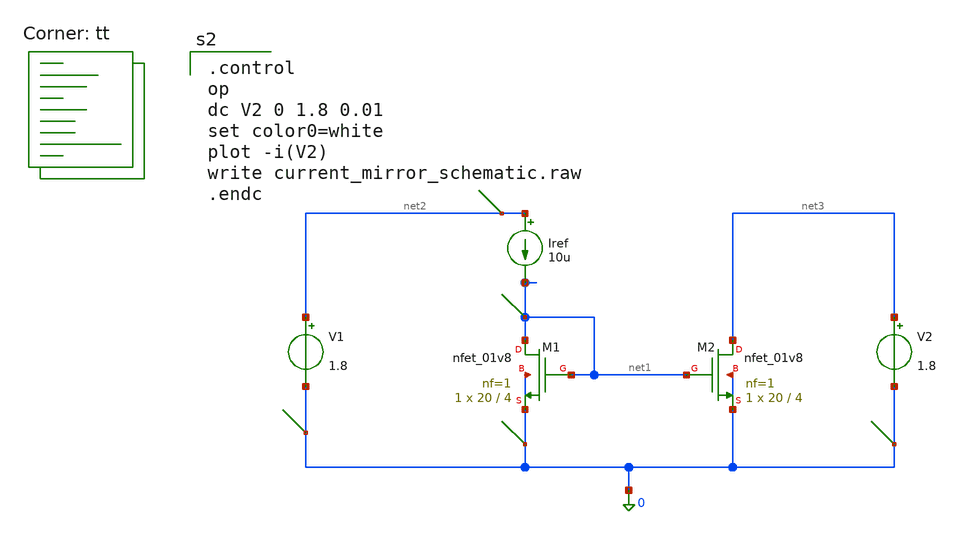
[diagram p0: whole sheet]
** sch_path: 01_schematic/current_mirror_schematic.sch
**.subckt current_mirror_schematic
XM1 net1 net1 0 0 sky130_fd_pr__nfet_01v8 L=4 W=20 nf=1 ad='int((1 + 1)/2) * 20 / 1 * 0.29' as='int((1 + 2)/2) * 20 / 1 * 0.29'
+ pd='2*int((1 + 1)/2) * (20 / 1 + 0.29)' ps='2*int((1 + 2)/2) * (20 / 1 + 0.29)' nrd='0.29 / 20 ' nrs='0.29 / 20 '
+ sa=0 sb=0 sd=0 mult=1 m=1
XM2 net3 net1 0 0 sky130_fd_pr__nfet_01v8 L=4 W=20 nf=1 ad='int((1 + 1)/2) * 20 / 1 * 0.29' as='int((1 + 2)/2) * 20 / 1 * 0.29'
+ pd='2*int((1 + 1)/2) * (20 / 1 + 0.29)' ps='2*int((1 + 2)/2) * (20 / 1 + 0.29)' nrd='0.29 / 20 ' nrs='0.29 / 20 '
+ sa=0 sb=0 sd=0 mult=1 m=1
Iref net2 net1 10u
V1 net2 0 1.8
V2 net3 0 1.8
**** begin user architecture code
.lib $::SKYWATER_MODELS/sky130.lib.spice tt

.control
op
dc V2 0 1.8 0.01
set color0=white
plot -i(V2)
write current_mirror_schematic.raw
.endc


**** end user architecture code
**.ends
.end
